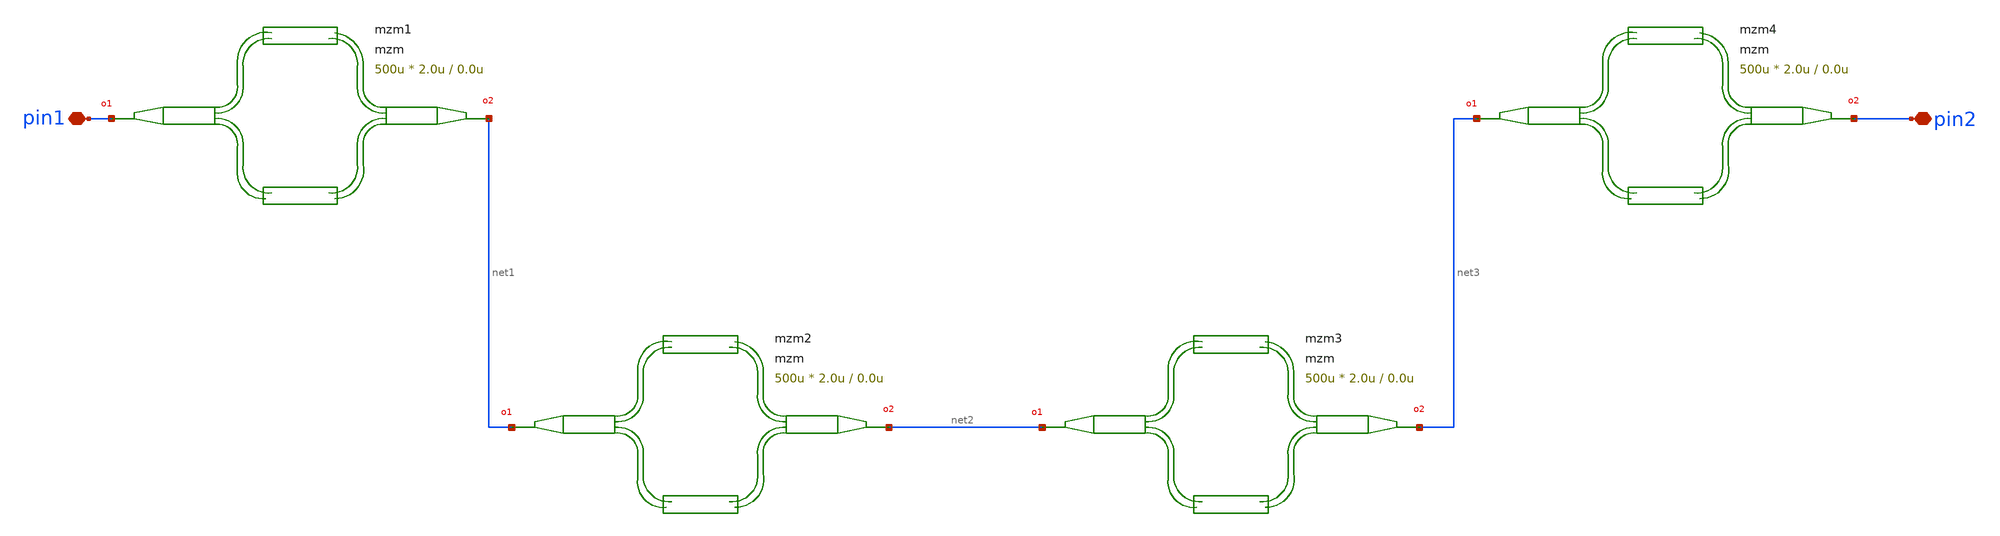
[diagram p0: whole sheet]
** sch_path: xschem/tests/test_sch/test_mzm.sch
* Copyright (c) 2024, Mabrains LLC
* Licensed under the GNU Lesser General Public License, Version 3.0 (the "License");
* you may not use this file except in compliance with the License.
* GNU Lesser General Public License
* Version 3, 29 June 2007
* This program is free software: you can redistribute it and/or modify
* it under the terms of the GNU Lesser General Public License as published
* by the Free Software Foundation, either version 3 of the License, or
* (at your option) any later version.
* This program is distributed in the hope that it will be useful,
* but WITHOUT ANY WARRANTY; without even the implied warranty of
* MERCHANTABILITY or FITNESS FOR A PARTICULAR PURPOSE.  See the
* GNU Lesser General Public License for more details.
* You should have received a copy of the GNU Lesser General Public License
* along with this program.  If not, see <https://www.gnu.org/licenses/>.
* SPDX-License-Identifier: LGPL-3.0
**.subckt test_mzm pin1 pin2
*.iopin pin1
*.iopin pin2
Pmzm2 net1 net2 mzm length_x=500u length_y=2.0u delta_length=0.0u
Pmzm1 pin1 net1 mzm length_x=500u length_y=2.0u delta_length=0.0u
Pmzm3 net2 net3 mzm length_x=500u length_y=2.0u delta_length=0.0u
Pmzm4 net3 pin2 mzm length_x=500u length_y=2.0u delta_length=0.0u
**.ends
.end
